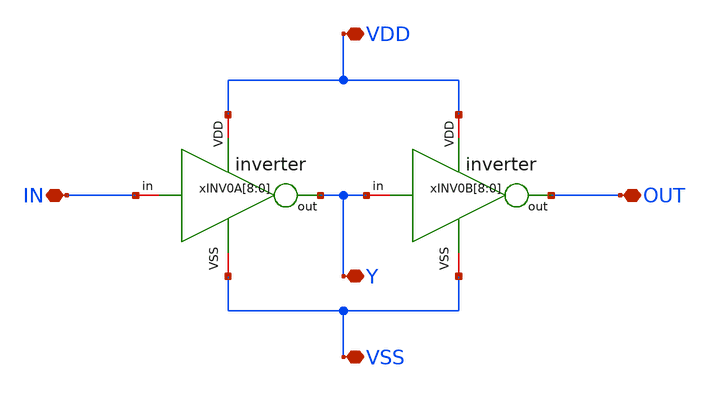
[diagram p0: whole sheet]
** sch_path: designs/sar_adc/digital/buffer_x1/xschem/buffer_SW0.sch
**.subckt buffer_SW0 OUT VSS VDD IN Y
*.iopin OUT
*.iopin VSS
*.iopin VDD
*.iopin IN
*.iopin Y
xINV0A[8] VDD IN Y VSS inverter
xINV0A[7] VDD IN Y VSS inverter
xINV0A[6] VDD IN Y VSS inverter
xINV0A[5] VDD IN Y VSS inverter
xINV0A[4] VDD IN Y VSS inverter
xINV0A[3] VDD IN Y VSS inverter
xINV0A[2] VDD IN Y VSS inverter
xINV0A[1] VDD IN Y VSS inverter
xINV0A[0] VDD IN Y VSS inverter
xINV0B[8] VDD Y OUT VSS inverter
xINV0B[7] VDD Y OUT VSS inverter
xINV0B[6] VDD Y OUT VSS inverter
xINV0B[5] VDD Y OUT VSS inverter
xINV0B[4] VDD Y OUT VSS inverter
xINV0B[3] VDD Y OUT VSS inverter
xINV0B[2] VDD Y OUT VSS inverter
xINV0B[1] VDD Y OUT VSS inverter
xINV0B[0] VDD Y OUT VSS inverter
**.ends

* expanding   symbol:  designs/sar_adc/digital/buffer_inv_x1/xschem/inverter.sym # of pins=6
** sym_path: designs/sar_adc/digital/buffer_inv_x1/xschem/inverter.sym
** sch_path: designs/sar_adc/digital/buffer_inv_x1/xschem/inverter.sch
.subckt inverter VDD in out VSS
*.opin out
*.iopin in
*.iopin VDD
*.iopin VSS
XM1 out in VSS VSS nfet_03v3 L=0.56u W=0.25u nf=1 ad='int((nf+1)/2) * W/nf * 0.18u' as='int((nf+2)/2) * W/nf * 0.18u'
+ pd='2*int((nf+1)/2) * (W/nf + 0.18u)' ps='2*int((nf+2)/2) * (W/nf + 0.18u)' nrd='0.18u / W' nrs='0.18u / W'
+ sa=0 sb=0 sd=0 m=2
XM2 out in VDD VDD pfet_03v3 L=0.56u W=0.25u nf=1 ad='int((nf+1)/2) * W/nf * 0.18u' as='int((nf+2)/2) * W/nf * 0.18u'
+ pd='2*int((nf+1)/2) * (W/nf + 0.18u)' ps='2*int((nf+2)/2) * (W/nf + 0.18u)' nrd='0.18u / W' nrs='0.18u / W'
+ sa=0 sb=0 sd=0 m=4
.ends

.end
